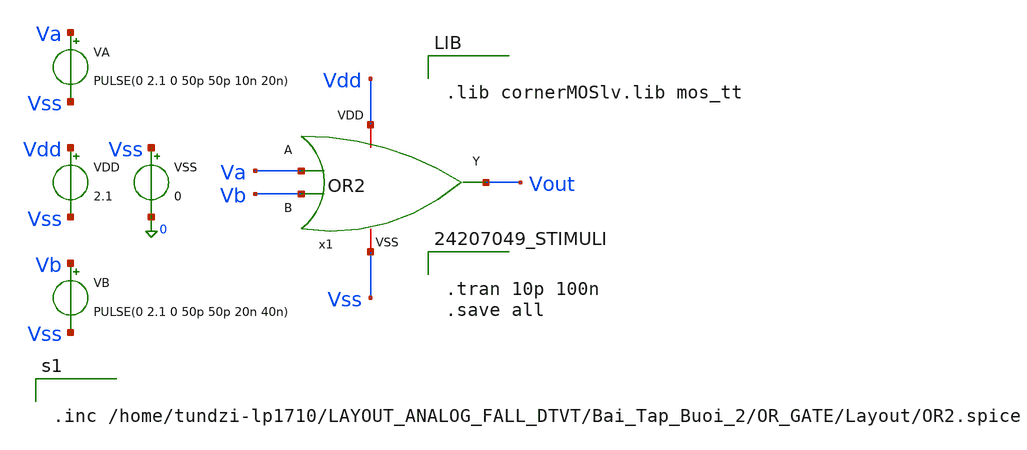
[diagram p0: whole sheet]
** sch_path: logic_gate/OR2/LAYOUT_POST-SIMULATION/OR2_tb.sch
**.subckt OR2_tb
VDD Vdd Vss 2.1
VSS Vss 0 0
VA Va Vss PULSE(0 2.1 0 50p 50p 10n 20n)
VB Vb Vss PULSE(0 2.1 0 50p 50p 20n 40n)
x1 Vdd Va Vb Vout Vss OR2
**** begin user architecture code


.tran 10p 100n
.save all




.lib cornerMOSlv.lib mos_tt




.inc /home/tundzi-lp1710/LAYOUT_ANALOG_FALL_DTVT/Bai_Tap_Buoi_2/OR_GATE/Layout/OR2.spice


**** end user architecture code
**.ends
.end
